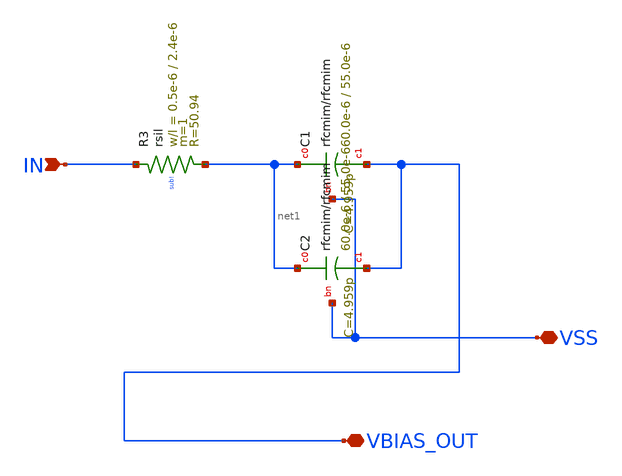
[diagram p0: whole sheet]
** sch_path: GPS_LNA/design_data/lvs/parts/inp.sch
**.subckt inp IN VSS VBIAS_OUT
*.ipin IN
*.iopin VSS
*.iopin VBIAS_OUT
XR3 IN net1 sub! rsil w=0.5e-6 l=2.4e-6 m=1 mm_ok=1
XC1 net1 VBIAS_OUT VSS rfcmim w=60.0e-6 l=55.0e-6 wfeed=5.0e-6 m=1 mm_ok=1
XC2 net1 VBIAS_OUT VSS rfcmim w=60.0e-6 l=55.0e-6 wfeed=5.0e-6 m=1 mm_ok=1
**.ends
.end
